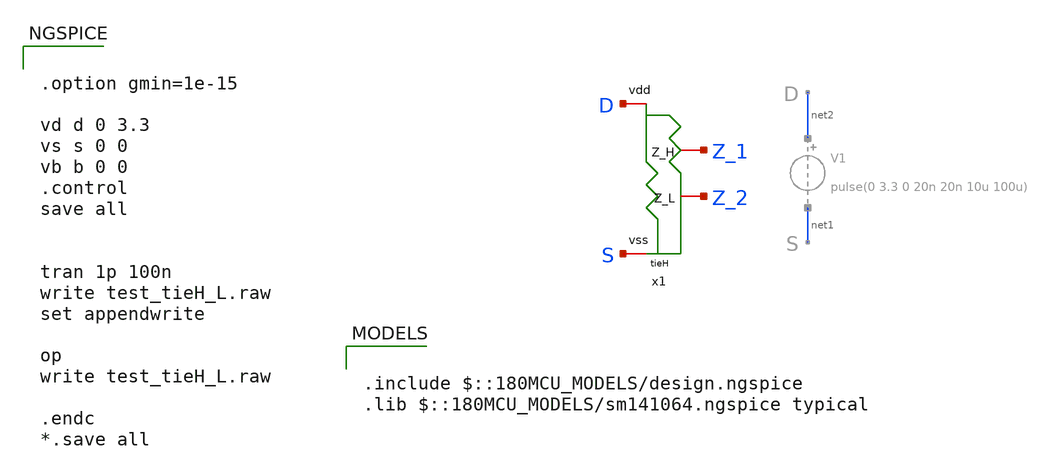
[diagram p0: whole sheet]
** sch_path: designs/libs/tb_TieL_TieH/test_tieH_L.sch
**.subckt test_tieH_L
x1 D S Z_1 Z_2 tieH
**** begin user architecture code

.include $::180MCU_MODELS/design.ngspice
.lib $::180MCU_MODELS/sm141064.ngspice typical



.option gmin=1e-15

vd d 0 3.3
vs s 0 0
vb b 0 0
.control
save all


tran 1p 100n
write test_tieH_L.raw
set appendwrite

op
write test_tieH_L.raw

.endc
*.save all


**** end user architecture code
**.ends
.end
